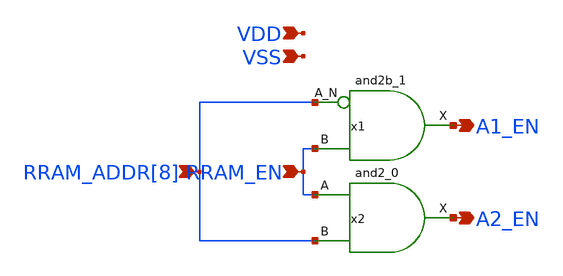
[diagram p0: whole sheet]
** sch_path: Top_Level_Array/subarray_enable_mux_assembly.sch
**.subckt subarray_enable_mux_assembly VSS VDD RRAM_EN RRAM_ADDR[8] A1_EN A2_EN
*.ipin VSS
*.ipin VDD
*.ipin RRAM_EN
*.ipin RRAM_ADDR[8]
*.opin A1_EN
*.opin A2_EN
x1 RRAM_ADDR[8] RRAM_EN VSS VSS VDD VDD A1_EN sky130_fd_sc_hd__and2b_1
x2 RRAM_EN RRAM_ADDR[8] VSS VSS VDD VDD A2_EN sky130_fd_sc_hd__and2_0
**.ends
.end
